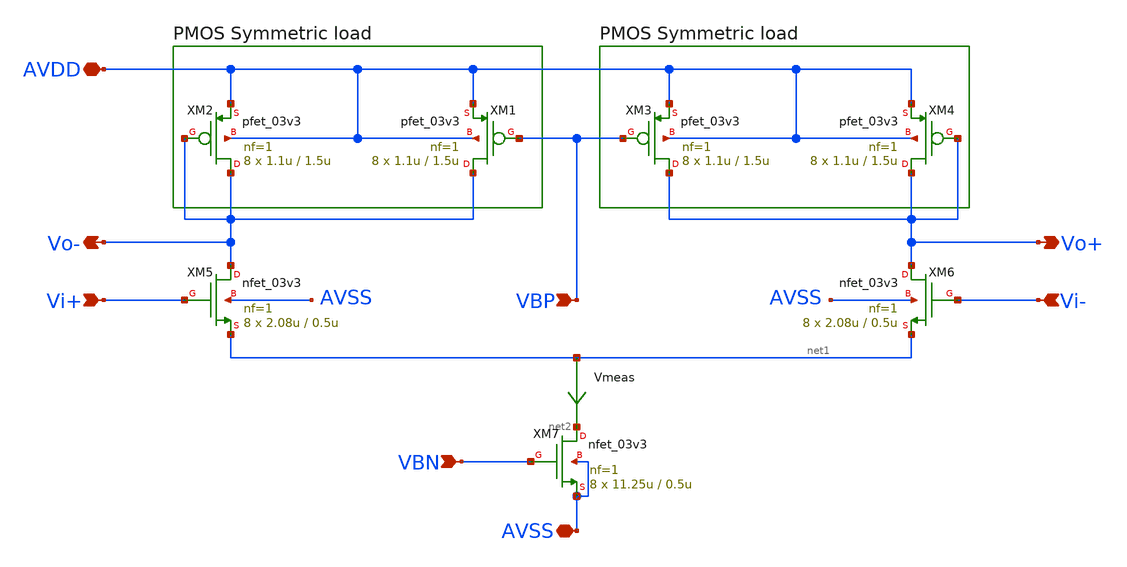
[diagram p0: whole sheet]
** sch_path: designs/libs/core_analog/delay_stage/delay_stage.sch
**.subckt delay_stage Vi+ Vi- Vo+ Vo- AVDD AVSS VBP VBN
*.ipin Vi+
*.ipin Vi-
*.opin Vo+
*.opin Vo-
*.iopin AVDD
*.iopin AVSS
*.ipin VBP
*.ipin VBN
XM7 net2 VBN AVSS AVSS nfet_03v3 L=0.5u W=11.25u nf=1 ad='int((nf+1)/2) * W/nf * 0.18u' as='int((nf+2)/2) * W/nf * 0.18u'
+ pd='2*int((nf+1)/2) * (W/nf + 0.18u)' ps='2*int((nf+2)/2) * (W/nf + 0.18u)' nrd='0.18u / W' nrs='0.18u / W'
+ sa=0 sb=0 sd=0 m=8
XM5 Vo- Vi+ net1 AVSS nfet_03v3 L=0.5u W=2.08u nf=1 ad='int((nf+1)/2) * W/nf * 0.18u' as='int((nf+2)/2) * W/nf * 0.18u'
+ pd='2*int((nf+1)/2) * (W/nf + 0.18u)' ps='2*int((nf+2)/2) * (W/nf + 0.18u)' nrd='0.18u / W' nrs='0.18u / W'
+ sa=0 sb=0 sd=0 m=8
XM2 Vo- Vo- AVDD AVDD pfet_03v3 L=1.5u W=1.1u nf=1 ad='int((nf+1)/2) * W/nf * 0.18u' as='int((nf+2)/2) * W/nf * 0.18u'
+ pd='2*int((nf+1)/2) * (W/nf + 0.18u)' ps='2*int((nf+2)/2) * (W/nf + 0.18u)' nrd='0.18u / W' nrs='0.18u / W'
+ sa=0 sb=0 sd=0 m=8
XM6 Vo+ Vi- net1 AVSS nfet_03v3 L=0.5u W=2.08u nf=1 ad='int((nf+1)/2) * W/nf * 0.18u' as='int((nf+2)/2) * W/nf * 0.18u'
+ pd='2*int((nf+1)/2) * (W/nf + 0.18u)' ps='2*int((nf+2)/2) * (W/nf + 0.18u)' nrd='0.18u / W' nrs='0.18u / W'
+ sa=0 sb=0 sd=0 m=8
XM1 Vo- VBP AVDD AVDD pfet_03v3 L=1.5u W=1.1u nf=1 ad='int((nf+1)/2) * W/nf * 0.18u' as='int((nf+2)/2) * W/nf * 0.18u'
+ pd='2*int((nf+1)/2) * (W/nf + 0.18u)' ps='2*int((nf+2)/2) * (W/nf + 0.18u)' nrd='0.18u / W' nrs='0.18u / W'
+ sa=0 sb=0 sd=0 m=8
XM3 Vo+ VBP AVDD AVDD pfet_03v3 L=1.5u W=1.1u nf=1 ad='int((nf+1)/2) * W/nf * 0.18u' as='int((nf+2)/2) * W/nf * 0.18u'
+ pd='2*int((nf+1)/2) * (W/nf + 0.18u)' ps='2*int((nf+2)/2) * (W/nf + 0.18u)' nrd='0.18u / W' nrs='0.18u / W'
+ sa=0 sb=0 sd=0 m=8
XM4 Vo+ Vo+ AVDD AVDD pfet_03v3 L=1.5u W=1.1u nf=1 ad='int((nf+1)/2) * W/nf * 0.18u' as='int((nf+2)/2) * W/nf * 0.18u'
+ pd='2*int((nf+1)/2) * (W/nf + 0.18u)' ps='2*int((nf+2)/2) * (W/nf + 0.18u)' nrd='0.18u / W' nrs='0.18u / W'
+ sa=0 sb=0 sd=0 m=8
Vmeas net1 net2 0
.save i(vmeas)
**.ends
.end
